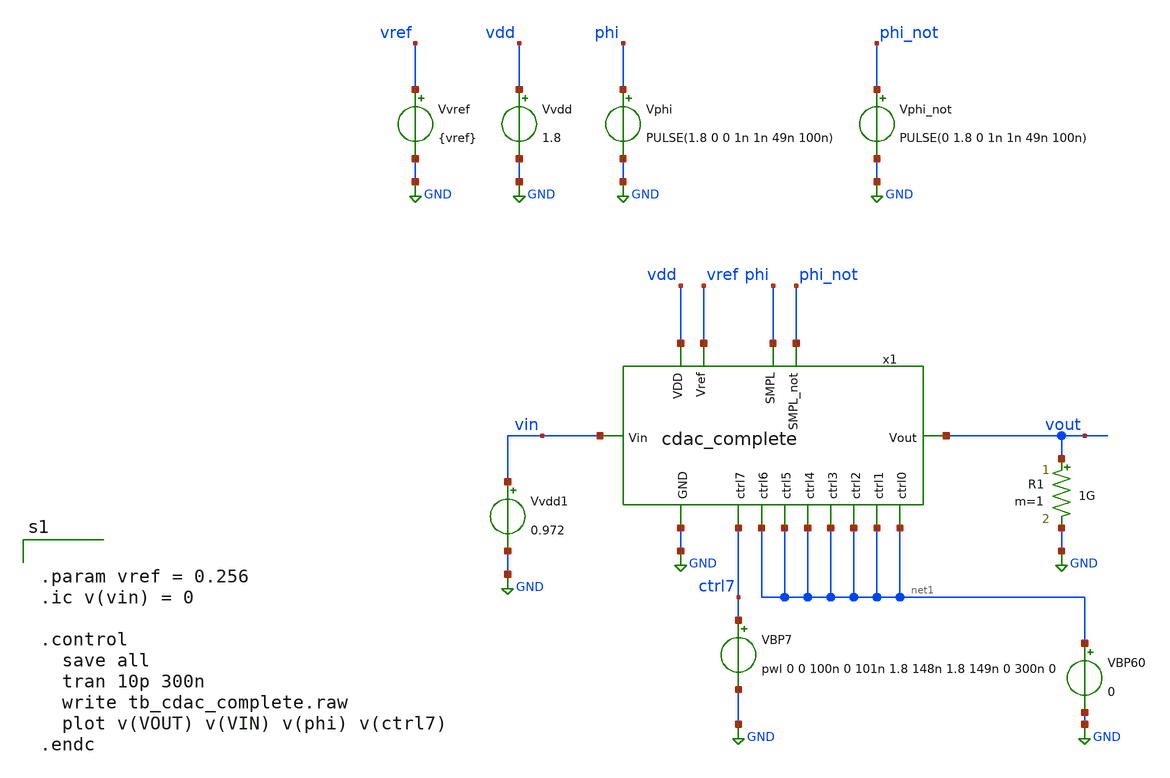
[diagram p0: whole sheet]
** sch_path: 05_mixed_signal/soluzioni/lab01/xschem/tb_cdac_complete.sch
**.subckt tb_cdac_complete
Vvdd vdd GND 1.8
Vvdd1 vin GND 0.972
Vphi phi GND PULSE(1.8 0 0 1n 1n 49n 100n)
Vphi_not phi_not GND PULSE(0 1.8 0 1n 1n 49n 100n)
Vvref vref GND {vref}
VBP7 ctrl7 GND pwl 0 0 100n 0 101n 1.8 148n 1.8 149n 0 300n 0
x1 vdd GND phi_not vout vin phi vref ctrl7 net1 net1 net1 net1 net1 net1 net1 cdac_complete
VBP60 net1 GND 0
R1 vout GND 1G m=1
**** begin user architecture code

** opencircuitdesign pdks install
.lib $::SKYWATER_MODELS/sky130.lib.spice tt



.param vref = 0.256
.ic v(vin) = 0

.control
  save all
  tran 10p 300n
  write tb_cdac_complete.raw
  plot v(VOUT) v(VIN) v(phi) v(ctrl7)
.endc


**** end user architecture code
**.ends
.GLOBAL GND
.end
